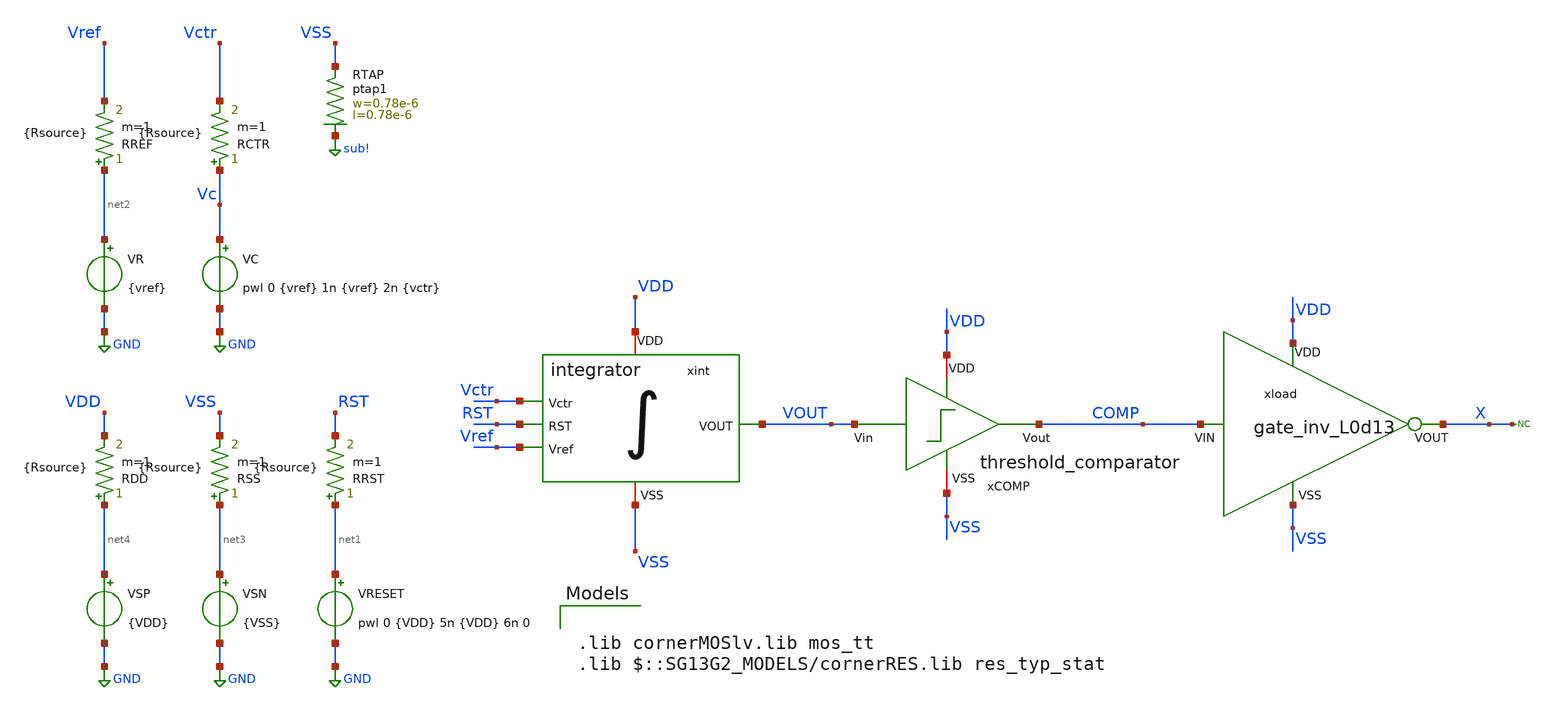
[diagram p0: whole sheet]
** sch_path: OSC9996-main/schematic/xschem/integrator_openloop.sch
**.subckt integrator_openloop
xint Vref VSS VDD RST Vctr VOUT integrator
VRESET net1 GND pwl 0 {VDD} 5n {VDD} 6n 0
VSN net3 GND {VSS}
VR net2 GND {vref}
VC Vc GND pwl 0 {vref} 1n {vref} 2n {vctr}
RDD net4 VDD {Rsource} m=1
RSS net3 VSS {Rsource} m=1
RRST net1 RST {Rsource} m=1
RREF net2 Vref {Rsource} m=1
RCTR Vc Vctr {Rsource} m=1
VSP net4 GND {VDD}
XRTAP VSS sub! ptap1 R=262.8 w=0.78e-6 l=0.78e-6
xCOMP VDD VOUT COMP VSS threshold_comparator
xload VDD COMP X VSS gate_inv_L0d13
* noconn X
**** begin user architecture code



.param Vctr = 1.2
.param Vref = 0.6
.param VDD = 1.2
.param VSS = 0
.param Rsource = 1

.save all

.control

* >> Variables <<
let Vhigh = 1.2
let Vmid = Vhigh * 0.5
let tstop = 50n
let tstep = tstop/10k

* Run transient analysis
tran $&tstep $&tstop

meas TRAN T_ctr TRIG v(xint.p1) VAL=Vmid rise=2 TARG v(xint.p1) VAL=Vmid rise=3
let F_ctr = 1 / T_ctr
meas TRAN T_ref TRIG v(xint.r1) VAL=Vmid rise=2 TARG v(xint.r1) VAL=Vmid rise=3
let F_ref = 1 / T_ref

print F_ctr F_ref

meas tran i_INT AVG i(VSP) from=$&tstep to=$&tstop
meas TRAN T_period TRIG v(xINT.R0) VAL=Vmid rise=2 TARG v(xINT.R0) VAL=Vmid rise=3
let i_INT_AVG=-1*i_INT

print i_INT_AVG

meas TRAN T_comp TRIG v(comp) VAL=Vmid rise=5 TARG v(comp) VAL=Vmid rise=6
let F_comp = 1 / T_comp

print F_comp

plot vout
plot xint.r1 xint.p1
plot comp

.endc



.lib cornerMOSlv.lib mos_tt
.lib $::SG13G2_MODELS/cornerRES.lib res_typ_stat

**** end user architecture code
**.ends
.GLOBAL GND
.GLOBAL sub!
.end
